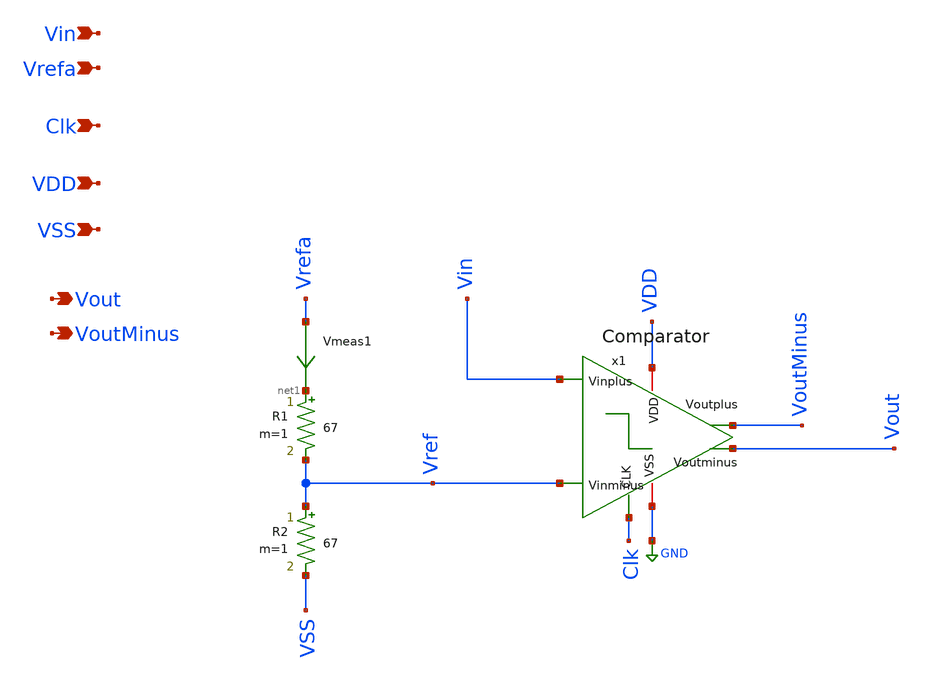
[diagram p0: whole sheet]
** sch_path: userLib/userLib/1bitADC.sch
**.subckt 1bitADC Vin Vrefa Clk VDD VSS Vout VoutMinus
*.ipin Vin
*.ipin Vrefa
*.ipin Clk
*.ipin VDD
*.ipin VSS
*.opin Vout
*.opin VoutMinus
x1 VDD Vout VoutMinus Clk Vin Vref GND Comparator
Vmeas1 Vrefa net1 0
.save i(vmeas1)
R1 net1 Vref 67 m=1
R2 Vref VSS 67 m=1
**.ends
.GLOBAL GND
.end
